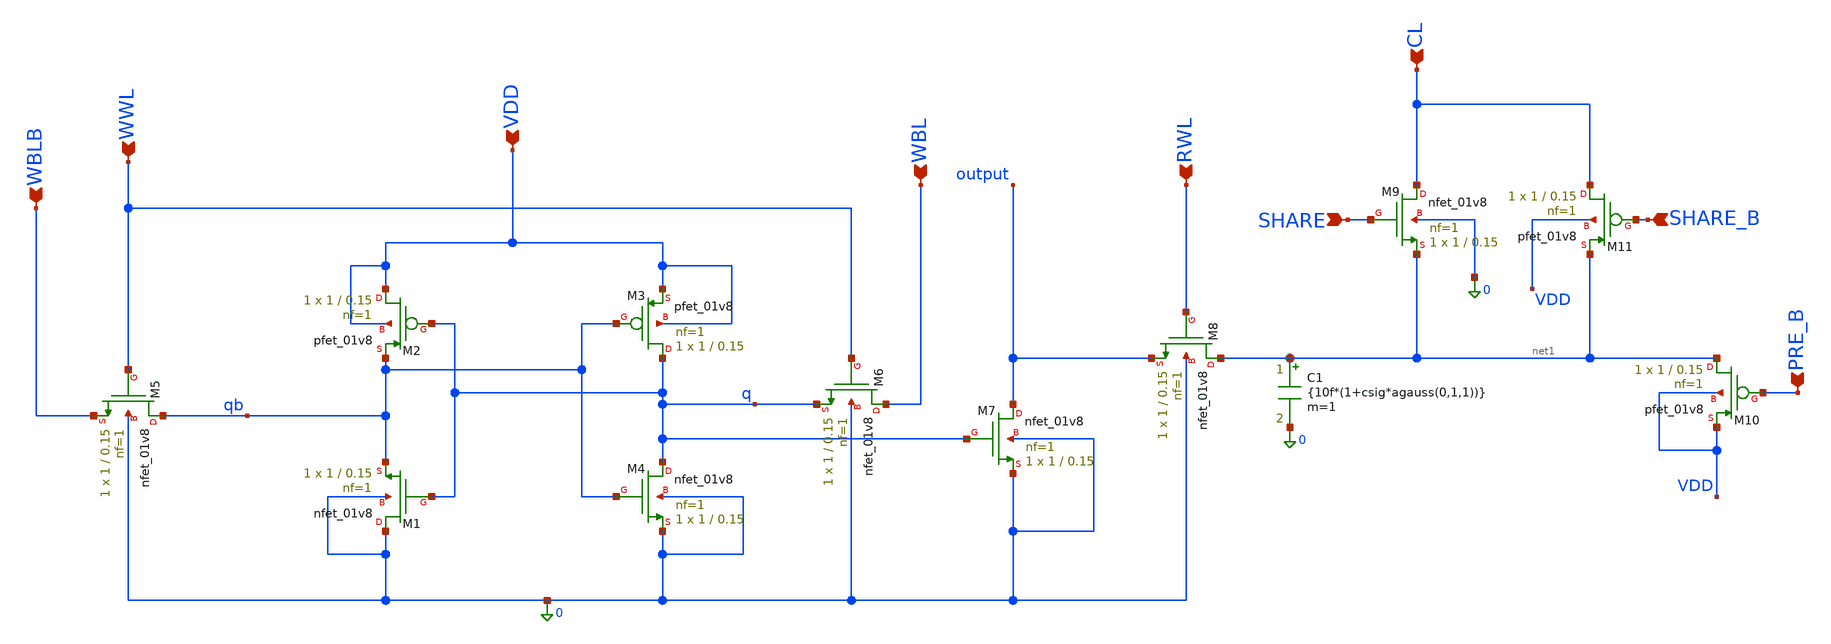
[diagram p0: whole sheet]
** sch_path: schematics/sram_8t_wcap.sch
**.subckt sram_8t_wcap WBLB WBL RWL WWL VDD PRE_B CL SHARE SHARE_B
*.ipin WBLB
*.ipin WBL
*.ipin RWL
*.ipin WWL
*.ipin VDD
*.ipin PRE_B
*.ipin CL
*.ipin SHARE
*.ipin SHARE_B
XM1 0 q qb 0 sky130_fd_pr__nfet_01v8 L=0.15 W=1 nf=1 ad='int((1 + 1)/2) * 1 / 1 * 0.29' as='int((1 + 2)/2) * 1 / 1 * 0.29'
+ pd='2*int((1 + 1)/2) * (1 / 1 + 0.29)' ps='2*int((1 + 2)/2) * (1 / 1 + 0.29)' nrd='0.29 / 1 ' nrs='0.29 / 1 '
+ sa=0 sb=0 sd=0 mult=1 m=1
XM2 VDD q qb VDD sky130_fd_pr__pfet_01v8 L=0.15 W=1 nf=1 ad='int((1 + 1)/2) * 1 / 1 * 0.29' as='int((1 + 2)/2) * 1 / 1 * 0.29'
+ pd='2*int((1 + 1)/2) * (1 / 1 + 0.29)' ps='2*int((1 + 2)/2) * (1 / 1 + 0.29)' nrd='0.29 / 1 ' nrs='0.29 / 1 '
+ sa=0 sb=0 sd=0 mult=1 m=1
XM3 q qb VDD VDD sky130_fd_pr__pfet_01v8 L=0.15 W=1 nf=1 ad='int((1 + 1)/2) * 1 / 1 * 0.29' as='int((1 + 2)/2) * 1 / 1 * 0.29'
+ pd='2*int((1 + 1)/2) * (1 / 1 + 0.29)' ps='2*int((1 + 2)/2) * (1 / 1 + 0.29)' nrd='0.29 / 1 ' nrs='0.29 / 1 '
+ sa=0 sb=0 sd=0 mult=1 m=1
XM4 q qb 0 0 sky130_fd_pr__nfet_01v8 L=0.15 W=1 nf=1 ad='int((1 + 1)/2) * 1 / 1 * 0.29' as='int((1 + 2)/2) * 1 / 1 * 0.29'
+ pd='2*int((1 + 1)/2) * (1 / 1 + 0.29)' ps='2*int((1 + 2)/2) * (1 / 1 + 0.29)' nrd='0.29 / 1 ' nrs='0.29 / 1 '
+ sa=0 sb=0 sd=0 mult=1 m=1
XM5 qb WWL WBLB 0 sky130_fd_pr__nfet_01v8 L=0.15 W=1 nf=1 ad='int((1 + 1)/2) * 1 / 1 * 0.29' as='int((1 + 2)/2) * 1 / 1 * 0.29'
+ pd='2*int((1 + 1)/2) * (1 / 1 + 0.29)' ps='2*int((1 + 2)/2) * (1 / 1 + 0.29)' nrd='0.29 / 1 ' nrs='0.29 / 1 '
+ sa=0 sb=0 sd=0 mult=1 m=1
XM6 WBL WWL q 0 sky130_fd_pr__nfet_01v8 L=0.15 W=1 nf=1 ad='int((1 + 1)/2) * 1 / 1 * 0.29' as='int((1 + 2)/2) * 1 / 1 * 0.29'
+ pd='2*int((1 + 1)/2) * (1 / 1 + 0.29)' ps='2*int((1 + 2)/2) * (1 / 1 + 0.29)' nrd='0.29 / 1 ' nrs='0.29 / 1 '
+ sa=0 sb=0 sd=0 mult=1 m=1
XM7 output q 0 0 sky130_fd_pr__nfet_01v8 L=0.15 W=1 nf=1 ad='int((1 + 1)/2) * 1 / 1 * 0.29' as='int((1 + 2)/2) * 1 / 1 * 0.29'
+ pd='2*int((1 + 1)/2) * (1 / 1 + 0.29)' ps='2*int((1 + 2)/2) * (1 / 1 + 0.29)' nrd='0.29 / 1 ' nrs='0.29 / 1 '
+ sa=0 sb=0 sd=0 mult=1 m=1
XM8 net1 RWL output 0 sky130_fd_pr__nfet_01v8 L=0.15 W=1 nf=1 ad='int((1 + 1)/2) * 1 / 1 * 0.29' as='int((1 + 2)/2) * 1 / 1 * 0.29'
+ pd='2*int((1 + 1)/2) * (1 / 1 + 0.29)' ps='2*int((1 + 2)/2) * (1 / 1 + 0.29)' nrd='0.29 / 1 ' nrs='0.29 / 1 '
+ sa=0 sb=0 sd=0 mult=1 m=1
C1 net1 0 {10f*(1+csig*agauss(0,1,1))} m=1
XM9 CL SHARE net1 0 sky130_fd_pr__nfet_01v8 L=0.15 W=1 nf=1 ad='int((1 + 1)/2) * 1 / 1 * 0.29' as='int((1 + 2)/2) * 1 / 1 * 0.29'
+ pd='2*int((1 + 1)/2) * (1 / 1 + 0.29)' ps='2*int((1 + 2)/2) * (1 / 1 + 0.29)' nrd='0.29 / 1 ' nrs='0.29 / 1 '
+ sa=0 sb=0 sd=0 mult=1 m=1
XM10 net1 PRE_B VDD VDD sky130_fd_pr__pfet_01v8 L=0.15 W=1 nf=1 ad='int((1 + 1)/2) * 1 / 1 * 0.29' as='int((1 + 2)/2) * 1 / 1 * 0.29'
+ pd='2*int((1 + 1)/2) * (1 / 1 + 0.29)' ps='2*int((1 + 2)/2) * (1 / 1 + 0.29)' nrd='0.29 / 1 ' nrs='0.29 / 1 '
+ sa=0 sb=0 sd=0 mult=1 m=1
XM11 CL SHARE_B net1 VDD sky130_fd_pr__pfet_01v8 L=0.15 W=1 nf=1 ad='int((1 + 1)/2) * 1 / 1 * 0.29' as='int((1 + 2)/2) * 1 / 1 * 0.29'
+ pd='2*int((1 + 1)/2) * (1 / 1 + 0.29)' ps='2*int((1 + 2)/2) * (1 / 1 + 0.29)' nrd='0.29 / 1 ' nrs='0.29 / 1 '
+ sa=0 sb=0 sd=0 mult=1 m=1
**.ends
.end
